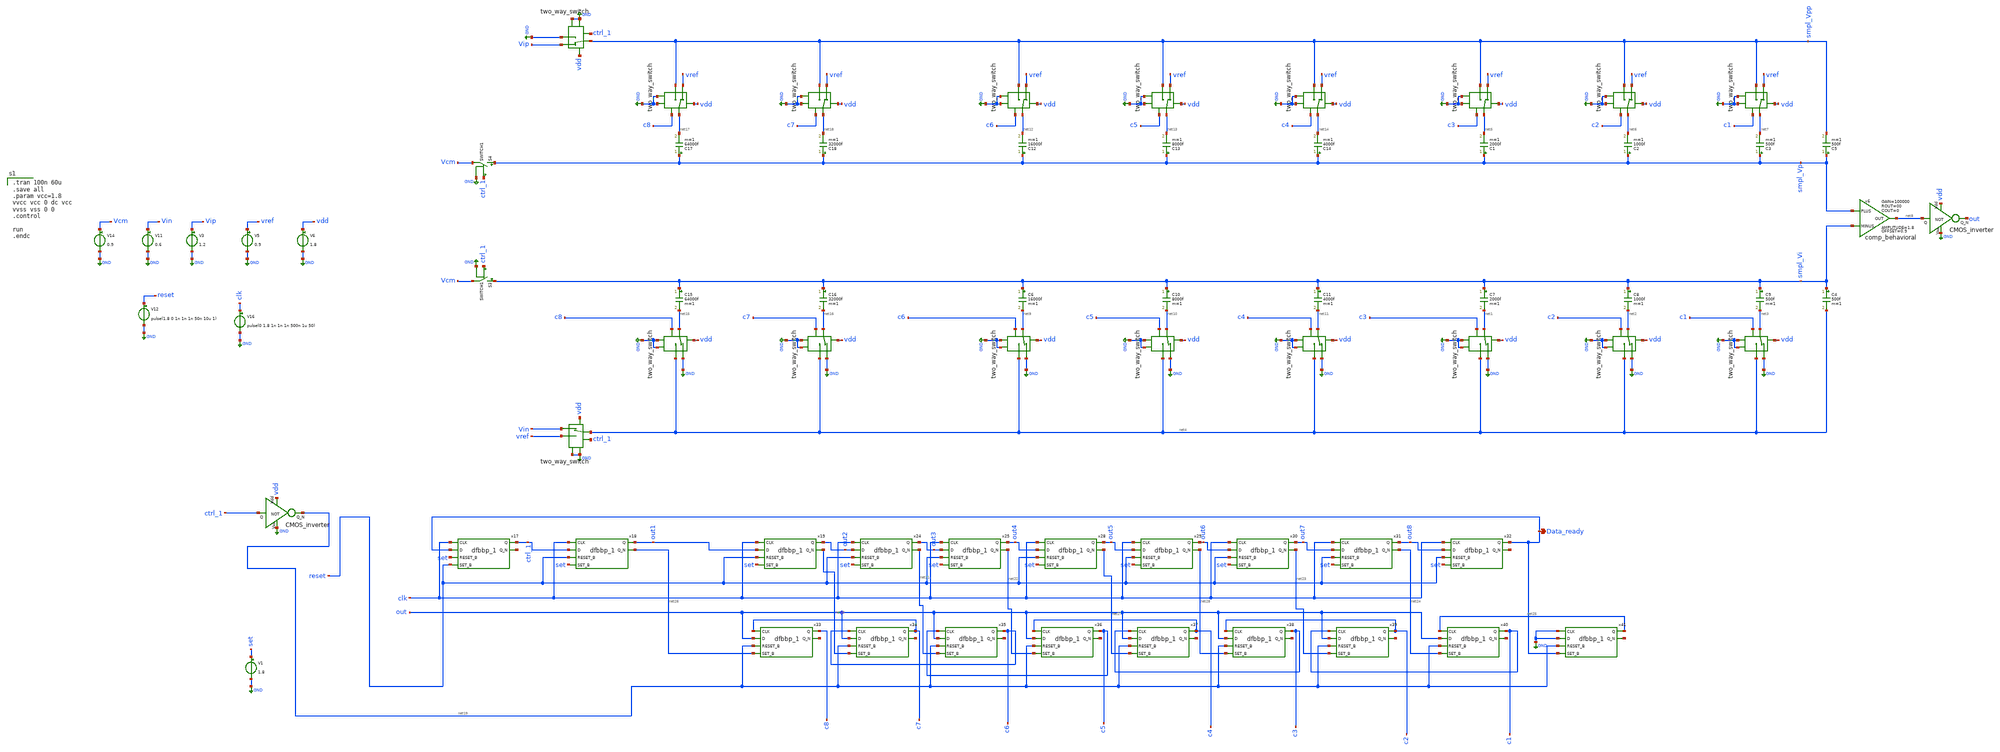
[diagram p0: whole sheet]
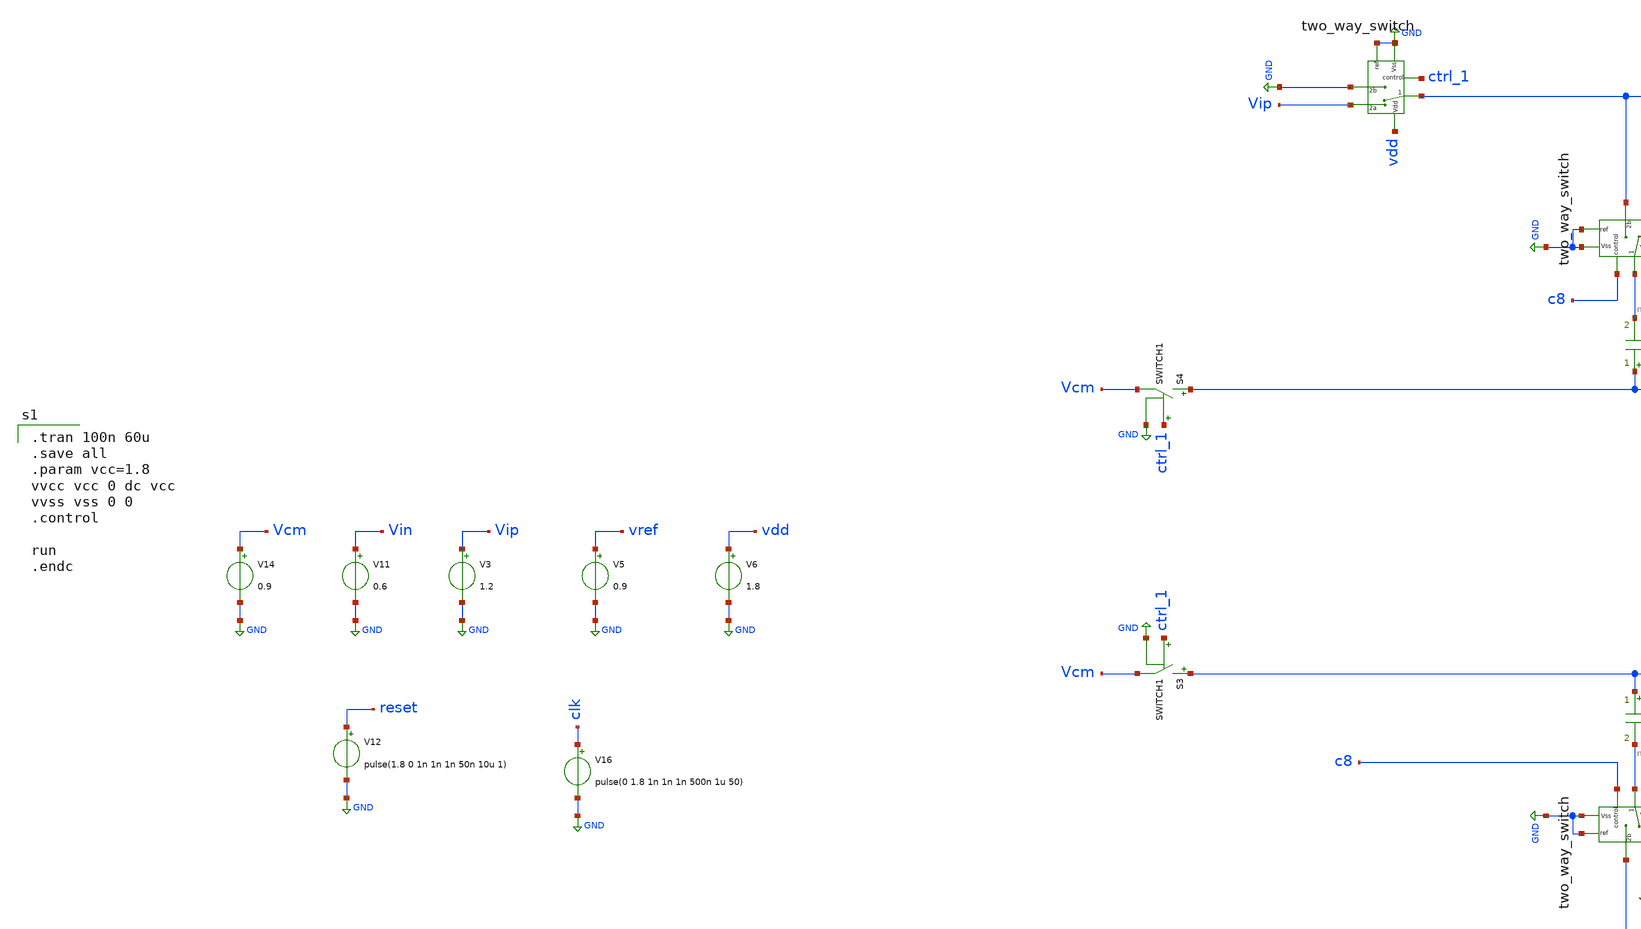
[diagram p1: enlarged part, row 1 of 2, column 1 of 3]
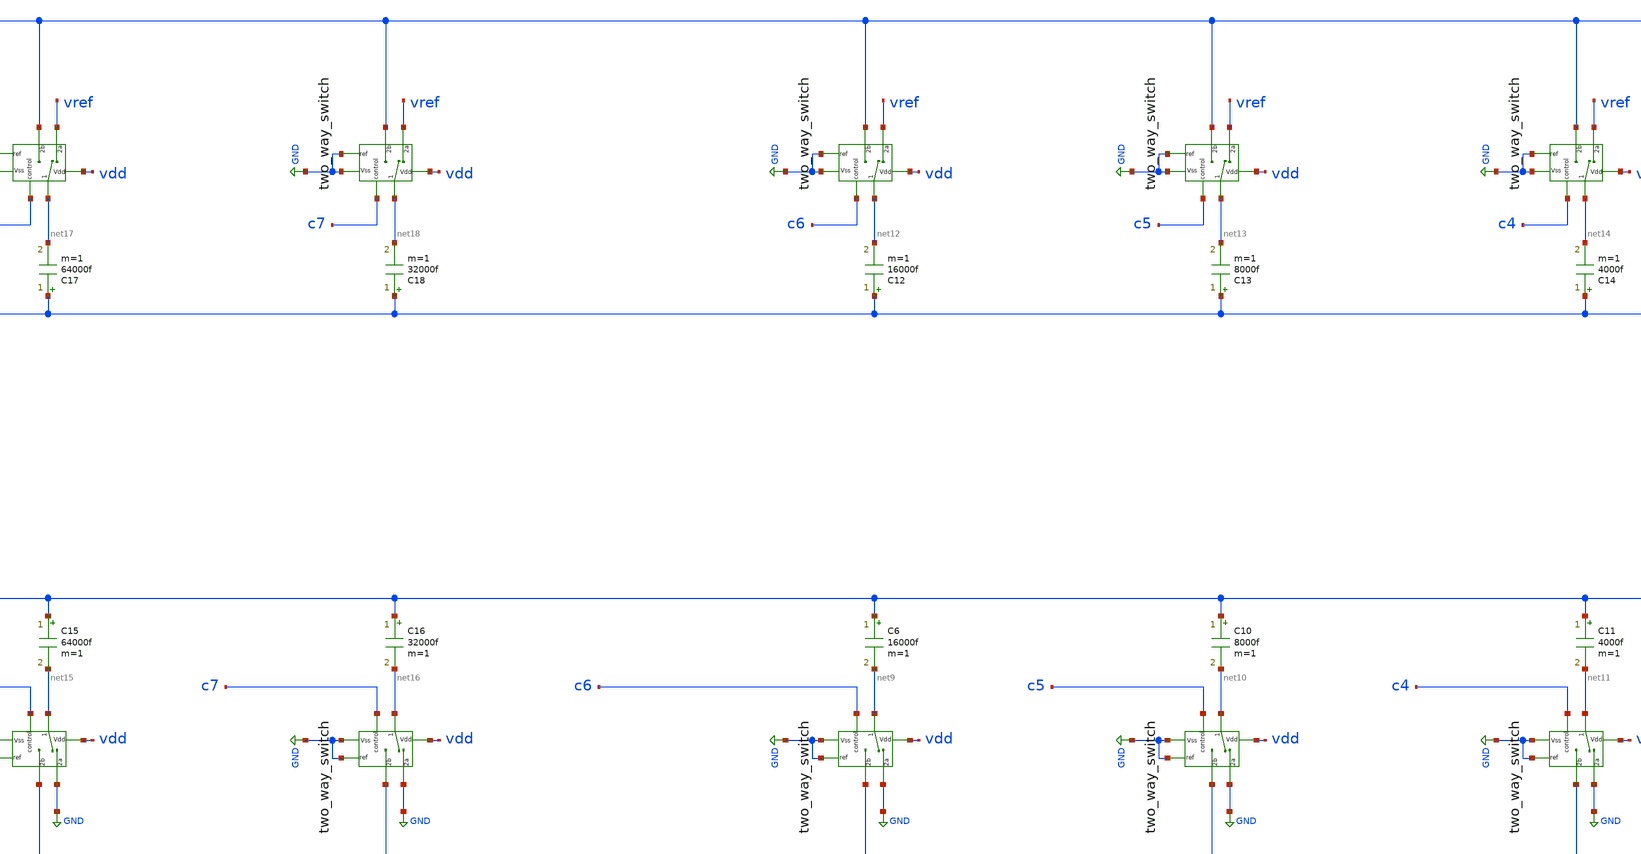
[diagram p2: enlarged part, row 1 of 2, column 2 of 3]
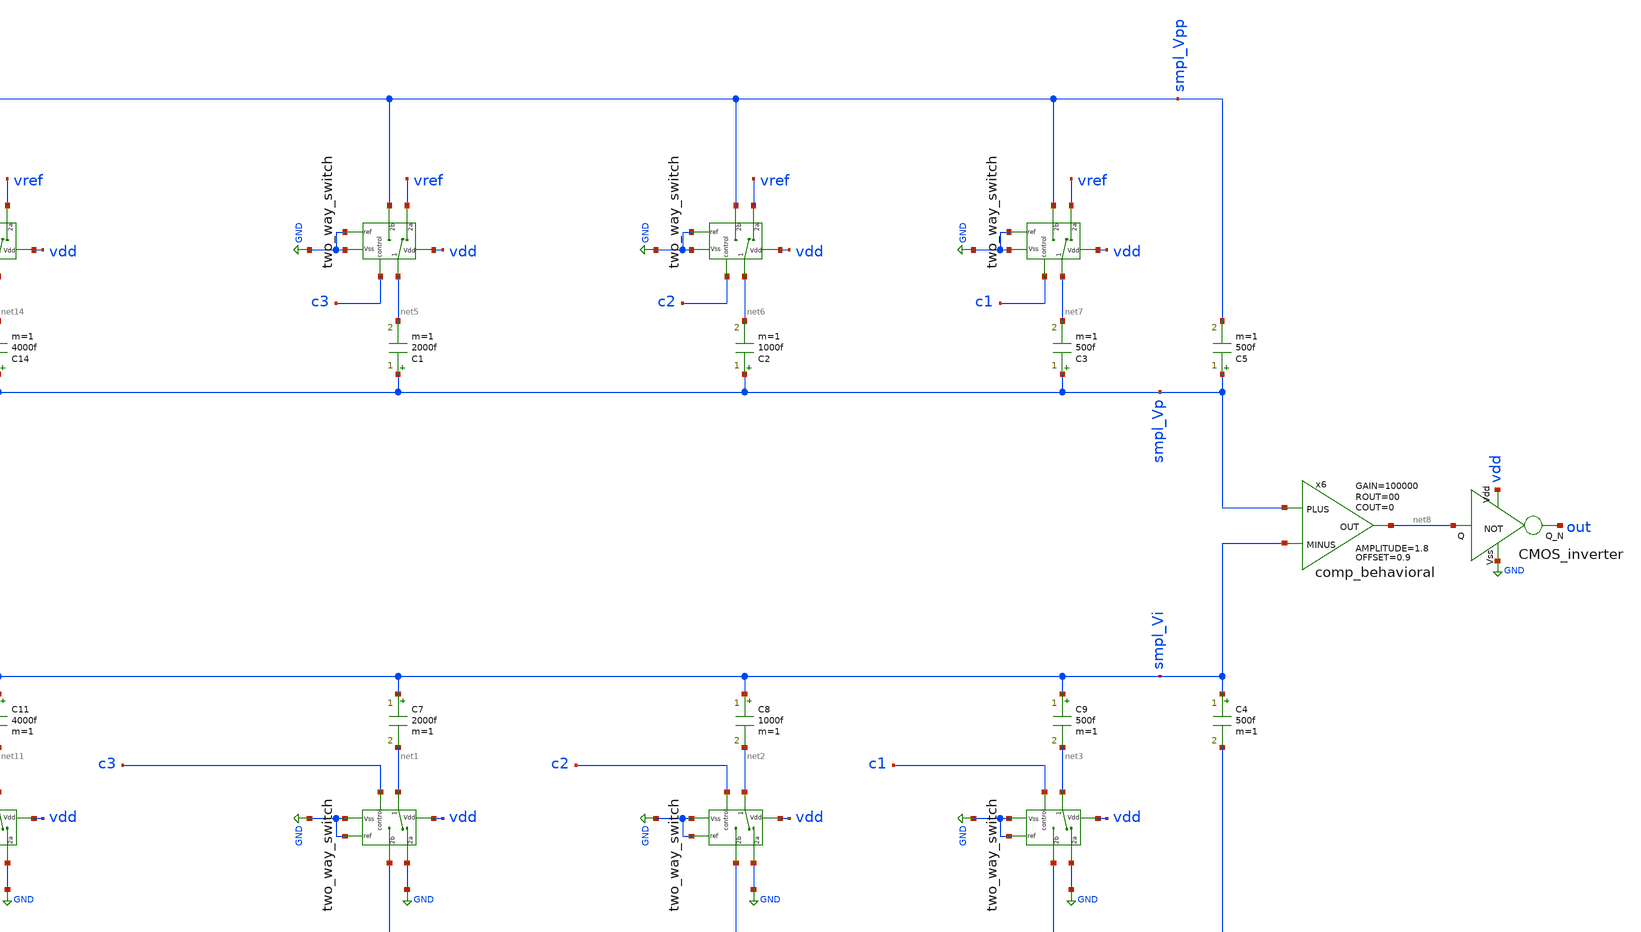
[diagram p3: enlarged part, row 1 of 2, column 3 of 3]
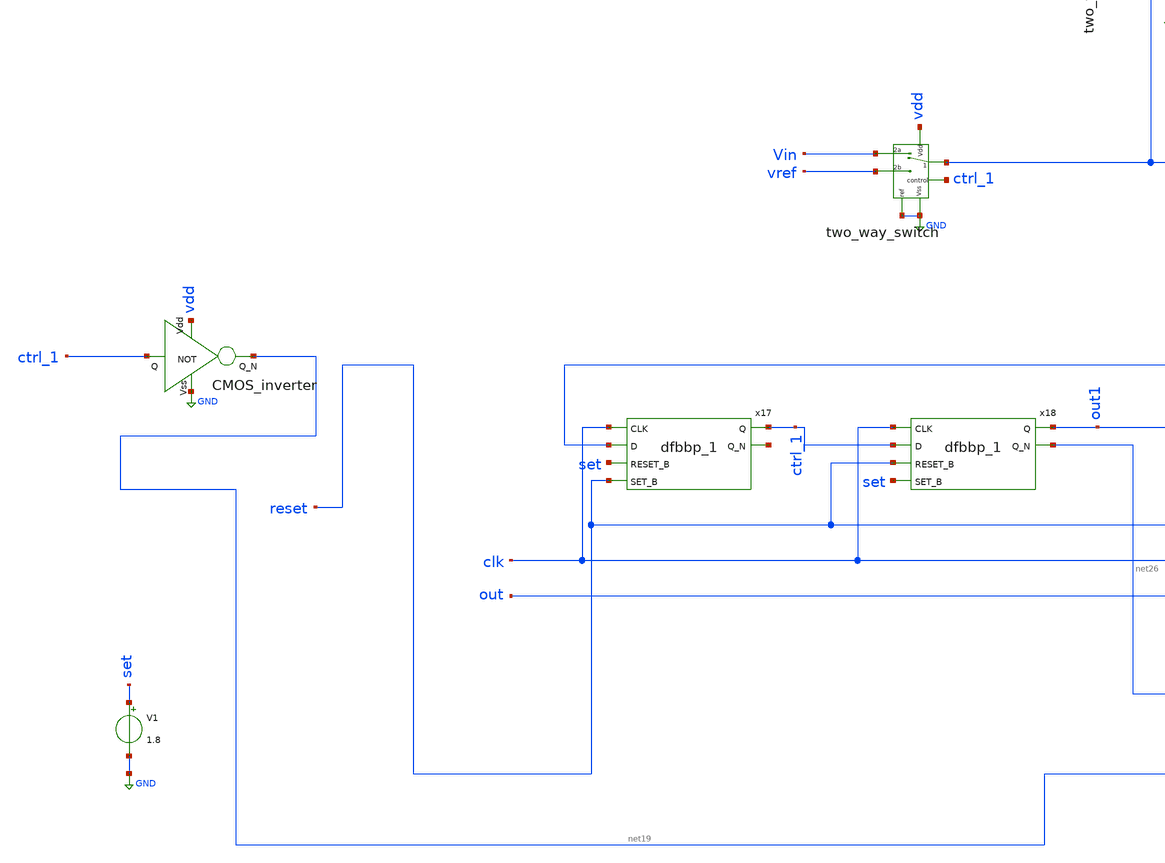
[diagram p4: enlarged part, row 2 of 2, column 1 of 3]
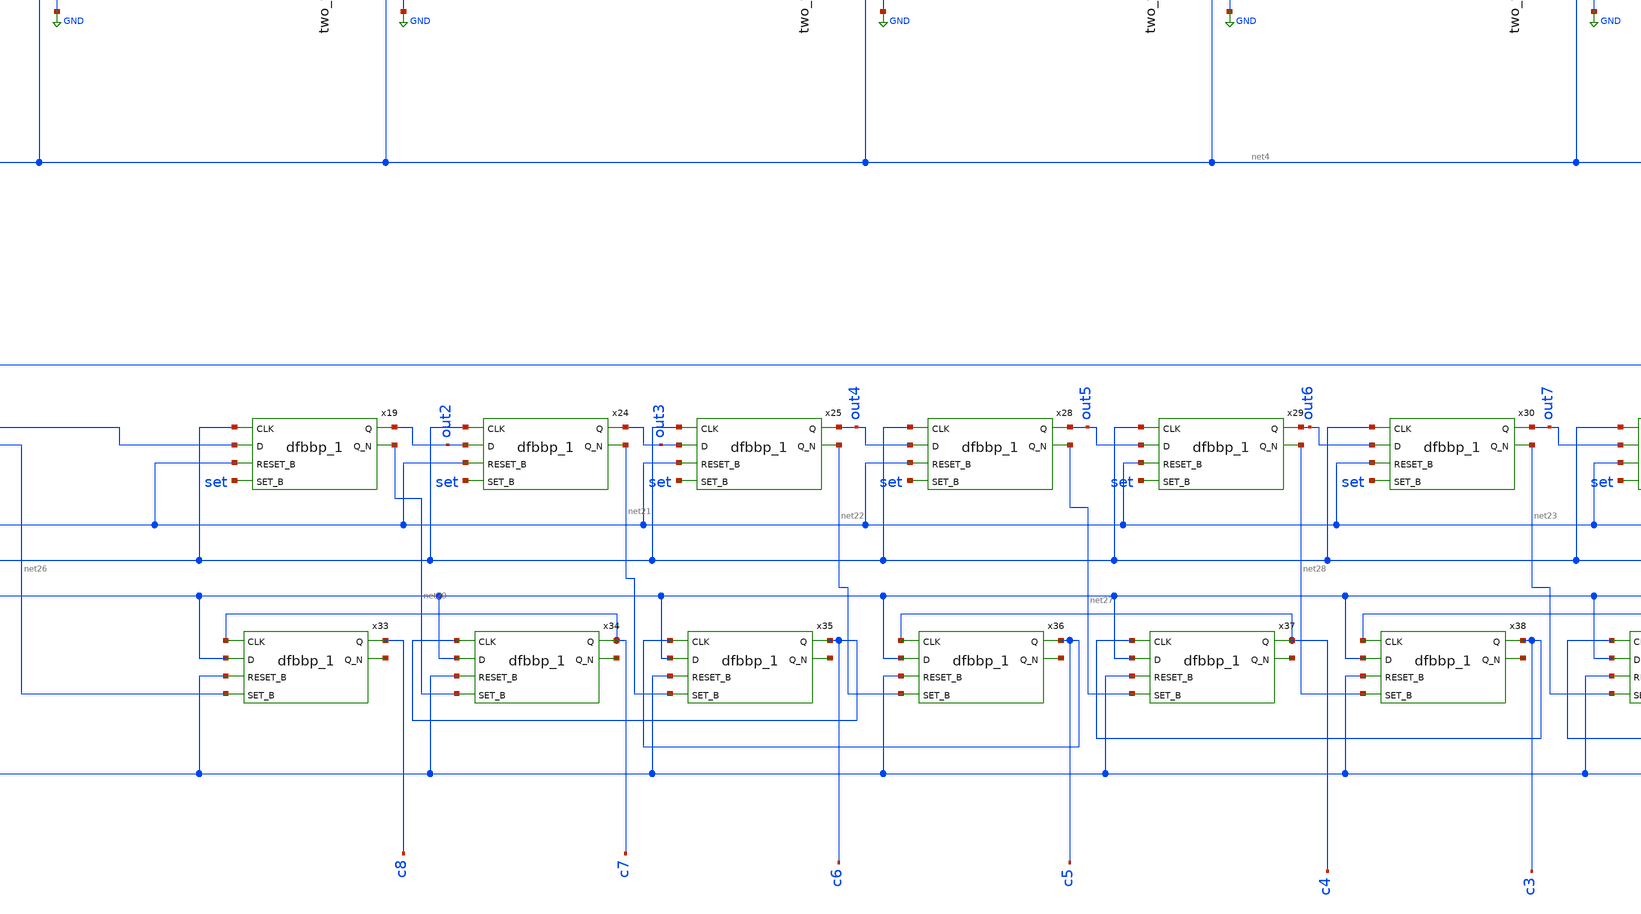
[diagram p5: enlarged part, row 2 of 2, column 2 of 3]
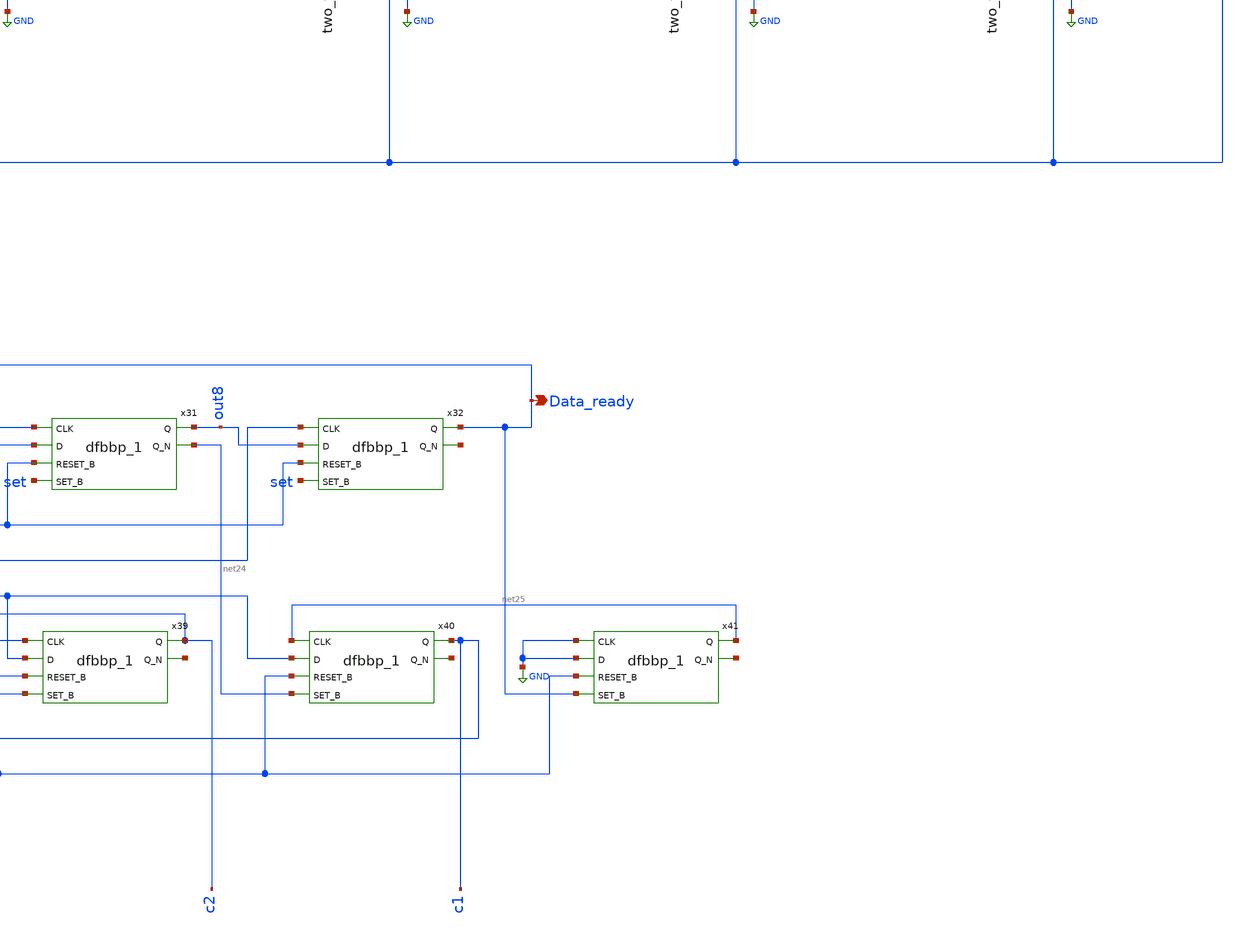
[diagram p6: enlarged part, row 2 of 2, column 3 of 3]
** sch_path: Behavioral_model/diff_mode_alternative_architecturee.sch
.lib $::SKYWATER_MODELS/sky130.lib.spice tt
.include $::SKYWATER_STDCELLS/sky130_fd_sc_hd.spice
.model switch1 sw vt=0.1 vh=0 ron=1 roff=100G

**.subckt diff_mode_alternative_architecturee Data_ready
*.opin Data_ready
S3 smpl_Vi Vcm ctrl_1 GND SWITCH1
V3 Vip GND 1.2
C7 smpl_Vi net1 2000f m=1
x7 net1 vdd c3 GND GND net4 GND two_way_switch
C8 smpl_Vi net2 1000f m=1
C9 smpl_Vi net3 500f m=1
x1 net2 vdd c2 GND GND net4 GND two_way_switch
x2 net3 vdd c1 GND GND net4 GND two_way_switch
V5 vref GND 0.9
V6 vdd GND 1.8
S4 smpl_Vp Vcm ctrl_1 GND SWITCH1
C1 smpl_Vp net5 2000f m=1
x3 net5 vdd c3 GND vref smpl_Vpp GND two_way_switch
C2 smpl_Vp net6 1000f m=1
C3 smpl_Vp net7 500f m=1
x4 net6 vdd c2 GND vref smpl_Vpp GND two_way_switch
x5 net7 vdd c1 GND vref smpl_Vpp GND two_way_switch
x6 smpl_Vp smpl_Vi net8 comp_behavioral OFFSET=0.9 AMPLITUDE=1.8 GAIN=100000 ROUT=00 COUT=0
V11 Vin GND 0.6
C4 smpl_Vi net4 500f m=1
C5 smpl_Vp smpl_Vpp 500f m=1
C6 smpl_Vi net9 16000f m=1
x11 net9 vdd c6 GND GND net4 GND two_way_switch
C10 smpl_Vi net10 8000f m=1
C11 smpl_Vi net11 4000f m=1
x12 net10 vdd c5 GND GND net4 GND two_way_switch
x13 net11 vdd c4 GND GND net4 GND two_way_switch
C12 smpl_Vp net12 16000f m=1
x14 net12 vdd c6 GND vref smpl_Vpp GND two_way_switch
C13 smpl_Vp net13 8000f m=1
C14 smpl_Vp net14 4000f m=1
x15 net13 vdd c5 GND vref smpl_Vpp GND two_way_switch
x16 net14 vdd c4 GND vref smpl_Vpp GND two_way_switch
C15 smpl_Vi net15 64000f m=1
x20 net15 vdd c8 GND GND net4 GND two_way_switch
C16 smpl_Vi net16 32000f m=1
x21 net16 vdd c7 GND GND net4 GND two_way_switch
C17 smpl_Vp net17 64000f m=1
x22 net17 vdd c8 GND vref smpl_Vpp GND two_way_switch
C18 smpl_Vp net18 32000f m=1
x23 net18 vdd c7 GND vref smpl_Vpp GND two_way_switch
x26 smpl_Vpp vdd ctrl_1 GND Vip GND GND two_way_switch
x27 net4 vdd ctrl_1 GND Vin vref GND two_way_switch
V14 Vcm GND 0.9
x9 vdd ctrl_1 net19 GND CMOS_inverter
V12 reset GND pulse(1.8 0 1n 1n 1n 50n 10u 1)
V16 clk GND pulse(0 1.8 1n 1n 1n 500n 1u 50)
x17 clk Data_ready set reset vss vss vcc vcc ctrl_1 net29 sky130_fd_sc_hd__dfbbp_1
x18 clk ctrl_1 reset set vss vss vcc vcc out1 net26 sky130_fd_sc_hd__dfbbp_1
x19 clk out1 reset set vss vss vcc vcc out2 net20 sky130_fd_sc_hd__dfbbp_1
x24 clk out2 reset set vss vss vcc vcc out3 net21 sky130_fd_sc_hd__dfbbp_1
x25 clk out3 reset set vss vss vcc vcc out4 net22 sky130_fd_sc_hd__dfbbp_1
x28 clk out4 reset set vss vss vcc vcc out5 net27 sky130_fd_sc_hd__dfbbp_1
x29 clk out5 reset set vss vss vcc vcc out6 net28 sky130_fd_sc_hd__dfbbp_1
x30 clk out6 reset set vss vss vcc vcc out7 net23 sky130_fd_sc_hd__dfbbp_1
x31 clk out7 reset set vss vss vcc vcc out8 net24 sky130_fd_sc_hd__dfbbp_1
x32 clk out8 reset set vss vss vcc vcc Data_ready net30 sky130_fd_sc_hd__dfbbp_1
x33 c7 out net19 net26 vss vss vcc vcc c8 net31 sky130_fd_sc_hd__dfbbp_1
x34 c6 out net19 net20 vss vss vcc vcc c7 net32 sky130_fd_sc_hd__dfbbp_1
x35 c5 out net19 net21 vss vss vcc vcc c6 net33 sky130_fd_sc_hd__dfbbp_1
x36 c4 out net19 net22 vss vss vcc vcc c5 net34 sky130_fd_sc_hd__dfbbp_1
x37 c3 out net19 net27 vss vss vcc vcc c4 net35 sky130_fd_sc_hd__dfbbp_1
x38 c2 out net19 net28 vss vss vcc vcc c3 net36 sky130_fd_sc_hd__dfbbp_1
x39 c1 out net19 net23 vss vss vcc vcc c2 net37 sky130_fd_sc_hd__dfbbp_1
x40 net25 out net19 net24 vss vss vcc vcc c1 net38 sky130_fd_sc_hd__dfbbp_1
x41 GND GND net19 Data_ready vss vss vcc vcc net25 net39 sky130_fd_sc_hd__dfbbp_1
V1 set GND 1.8
x10 vdd net8 out GND CMOS_inverter
**** begin user architecture code

.tran 100n 60u
.save all
.param vcc=1.8
vvcc vcc 0 dc vcc
vvss vss 0 0
.control

run
.endc

**** end user architecture code
**.ends

* expanding   symbol:  two_way_switch.sym # of pins=7
** sym_path: Behavioral_model/two_way_switch.sym
** sch_path: Behavioral_model/two_way_switch.sch
.subckt two_way_switch 1 Vdd control ref 2a 2b Vss
*.iopin 2b
*.iopin 2a
*.ipin ref
*.iopin 1
*.ipin Vdd
*.ipin Vss
*.ipin control
S1 1 2a control ref SWITCH1
S2 1 2b net1 ref SWITCH1
x1 Vdd control net1 Vss CMOS_inverter
.ends


* expanding   symbol:  comp_behavioral.sym # of pins=3
** sym_path: Behavioral_model/comp_behavioral.sym
** sch_path: Behavioral_model/comp_behavioral.sch
.subckt comp_behavioral PLUS MINUS OUT  OFFSET=0.9 AMPLITUDE=0.9 GAIN=100000 ROUT=00 COUT=0
*.ipin PLUS
*.ipin MINUS
*.opin OUT
B1 IOUT 0 V = {OFFSET + AMPLITUDE/2*(tanh(V(IPLUS,IMINUS)*GAIN*2/AMPLITUDE))}
V1 IPLUS PLUS 3
V2 IMINUS MINUS 3
R1 OUT IOUT {ROUT} m=1
C3 OUT 0 {COUT} m=1
.ends


* expanding   symbol:  CMOS_inverter.sym # of pins=4
** sym_path: Behavioral_model/CMOS_inverter.sym
** sch_path: Behavioral_model/CMOS_inverter.sch
.subckt CMOS_inverter Vdd Q Q_N Vss
*.ipin Q
*.ipin Vdd
*.ipin Vss
*.opin Q_N
XM1 Q_N Q Vss Vss sky130_fd_pr__nfet_01v8 L=0.15 W=1 nf=1 ad='int((nf+1)/2) * W/nf * 0.29' as='int((nf+2)/2) * W/nf * 0.29'
+ pd='2*int((nf+1)/2) * (W/nf + 0.29)' ps='2*int((nf+2)/2) * (W/nf + 0.29)' nrd='0.29 / W' nrs='0.29 / W'
+ sa=0 sb=0 sd=0 mult=1 m=1
XM3 Q_N Q Vdd Vdd sky130_fd_pr__pfet_01v8 L=0.15 W=1 nf=1 ad='int((nf+1)/2) * W/nf * 0.29' as='int((nf+2)/2) * W/nf * 0.29'
+ pd='2*int((nf+1)/2) * (W/nf + 0.29)' ps='2*int((nf+2)/2) * (W/nf + 0.29)' nrd='0.29 / W' nrs='0.29 / W'
+ sa=0 sb=0 sd=0 mult=1 m=1
.ends

.GLOBAL GND
.end
